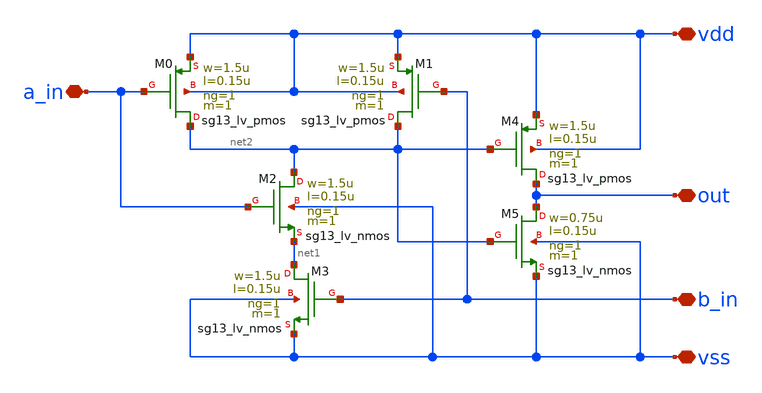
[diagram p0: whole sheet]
** sch_path: design/blocks/andgate/schematic/andgate.sch
**.subckt andgate b_in a_in out vdd vss
*.iopin b_in
*.iopin a_in
*.iopin out
*.iopin vdd
*.iopin vss
XM0 net2 a_in vdd vdd sg13_lv_pmos w=1.5u l=0.15u ng=1 m=1 mm_ok=1
XM1 net2 b_in vdd vdd sg13_lv_pmos w=1.5u l=0.15u ng=1 m=1 mm_ok=1
XM2 net2 a_in net1 vss sg13_lv_nmos w=1.5u l=0.15u ng=1 m=1 mm_ok=1
XM3 net1 b_in vss vss sg13_lv_nmos w=1.5u l=0.15u ng=1 m=1 mm_ok=1
XM4 out net2 vdd vdd sg13_lv_pmos w=1.5u l=0.15u ng=1 m=1 mm_ok=1
XM5 out net2 vss vss sg13_lv_nmos w=0.75u l=0.15u ng=1 m=1 mm_ok=1
**.ends
.end
